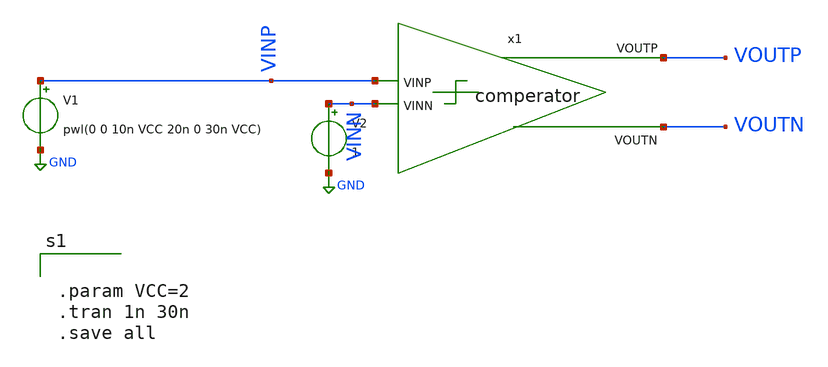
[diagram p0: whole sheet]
** sch_path: XSCHEM Files/comp_tb.sch
**.subckt comp_tb
V1 VINP GND pwl(0 0 10n VCC 20n 0 30n VCC)
V2 VINN GND 1
x1 VOUTP VINP VOUTN VINN comperator
**** begin user architecture code


.param VCC=2
.tran 1n 30n
.save all


**** end user architecture code
**.ends

* expanding   symbol:  /home/tare/Desktop/Final/comperator.sym # of pins=4
** sym_path: XSCHEM Files/comperator.sym
** sch_path: XSCHEM Files/comperator.sch
.subckt comperator VOUTP VINP VOUTN VINN
*.ipin VINP
*.opin VOUTP
*.ipin VINN
*.opin VOUTN
V1 VINPi VINP 0
V2 VINNi VINN 0
B2 VOUTN GND V = {VCC/2 + VCC/2 *(tanh(V(VINPi,VINNi)*1e6*-1))}
B1 VOUTP GND V = {VCC/2 + VCC/2 *(tanh(V(VINPi,VINNi)*1e6))}
.ends

.GLOBAL GND
.end
